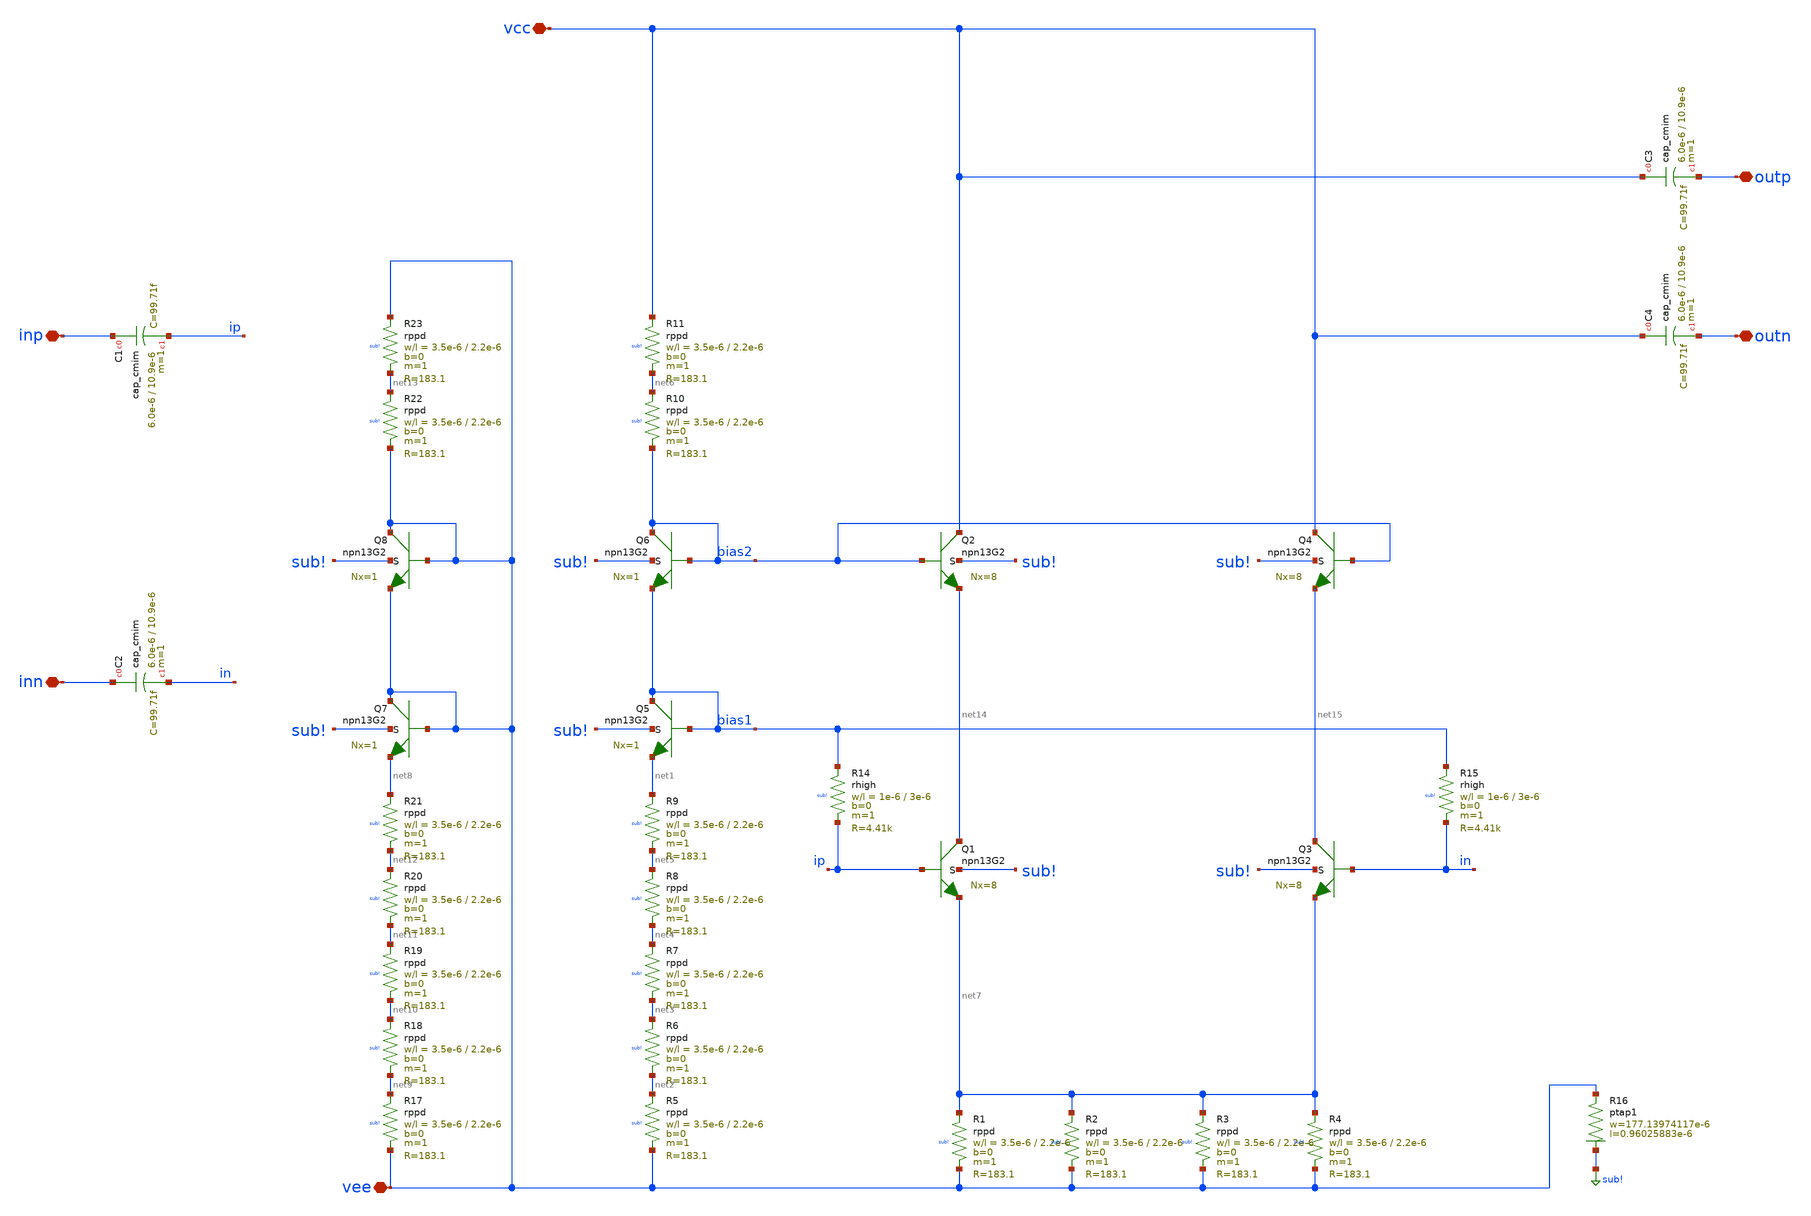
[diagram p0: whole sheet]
** sch_path: LNA0379-main/schematic/xschem/LNA0379_coreLVS.sch
**.subckt LNA0379_coreLVS inp inn vcc vee outp outn
*.iopin inp
*.iopin inn
*.iopin vcc
*.iopin vee
*.iopin outp
*.iopin outn
XQ1 net14 ip net7 sub! npn13G2 Nx=8 mm_ok=1
XQ2 vcc bias2 net14 sub! npn13G2 Nx=8 mm_ok=1
XQ3 net15 in net7 sub! npn13G2 Nx=8 mm_ok=1
XQ4 vcc bias2 net15 sub! npn13G2 Nx=8 mm_ok=1
XQ5 bias1 bias1 net1 sub! npn13G2 Nx=1 mm_ok=1
XQ6 bias2 bias2 bias1 sub! npn13G2 Nx=1 mm_ok=1
XR14 bias1 ip sub! rhigh w=1e-6 l=3e-6 m=1 b=0 mm_ok=1
XR15 bias1 in sub! rhigh w=1e-6 l=3e-6 m=1 b=0 mm_ok=1
XR1 net7 vee sub! rppd w=3.5e-6 l=2.2e-6 m=1 b=0 mm_ok=1
XR16 vee sub! ptap1 R=1.862 w=177.13974117e-6 l=0.96025883e-6
XQ7 vee vee net8 sub! npn13G2 Nx=1 mm_ok=1
XQ8 vee vee vee sub! npn13G2 Nx=1 mm_ok=1
XR2 net7 vee sub! rppd w=3.5e-6 l=2.2e-6 m=1 b=0 mm_ok=1
XR3 net7 vee sub! rppd w=3.5e-6 l=2.2e-6 m=1 b=0 mm_ok=1
XR4 net7 vee sub! rppd w=3.5e-6 l=2.2e-6 m=1 b=0 mm_ok=1
XR5 net2 vee sub! rppd w=3.5e-6 l=2.2e-6 m=1 b=0 mm_ok=1
XR6 net3 net2 sub! rppd w=3.5e-6 l=2.2e-6 m=1 b=0 mm_ok=1
XR7 net4 net3 sub! rppd w=3.5e-6 l=2.2e-6 m=1 b=0 mm_ok=1
XR8 net5 net4 sub! rppd w=3.5e-6 l=2.2e-6 m=1 b=0 mm_ok=1
XR9 net1 net5 sub! rppd w=3.5e-6 l=2.2e-6 m=1 b=0 mm_ok=1
XR10 net6 bias2 sub! rppd w=3.5e-6 l=2.2e-6 m=1 b=0 mm_ok=1
XR11 vcc net6 sub! rppd w=3.5e-6 l=2.2e-6 m=1 b=0 mm_ok=1
XR17 net9 vee sub! rppd w=3.5e-6 l=2.2e-6 m=1 b=0 mm_ok=1
XR18 net10 net9 sub! rppd w=3.5e-6 l=2.2e-6 m=1 b=0 mm_ok=1
XR19 net11 net10 sub! rppd w=3.5e-6 l=2.2e-6 m=1 b=0 mm_ok=1
XR20 net12 net11 sub! rppd w=3.5e-6 l=2.2e-6 m=1 b=0 mm_ok=1
XR21 net8 net12 sub! rppd w=3.5e-6 l=2.2e-6 m=1 b=0 mm_ok=1
XR22 net13 vee sub! rppd w=3.5e-6 l=2.2e-6 m=1 b=0 mm_ok=1
XR23 vee net13 sub! rppd w=3.5e-6 l=2.2e-6 m=1 b=0 mm_ok=1
XC1 inp ip cap_cmim w=6.0e-6 l=10.9e-6 m=1 mm_ok=1
XC2 inn in cap_cmim w=6.0e-6 l=10.9e-6 m=1 mm_ok=1
XC3 vcc outp cap_cmim w=6.0e-6 l=10.9e-6 m=1 mm_ok=1
XC4 vcc outn cap_cmim w=6.0e-6 l=10.9e-6 m=1 mm_ok=1
**.ends
.GLOBAL sub!
.end
